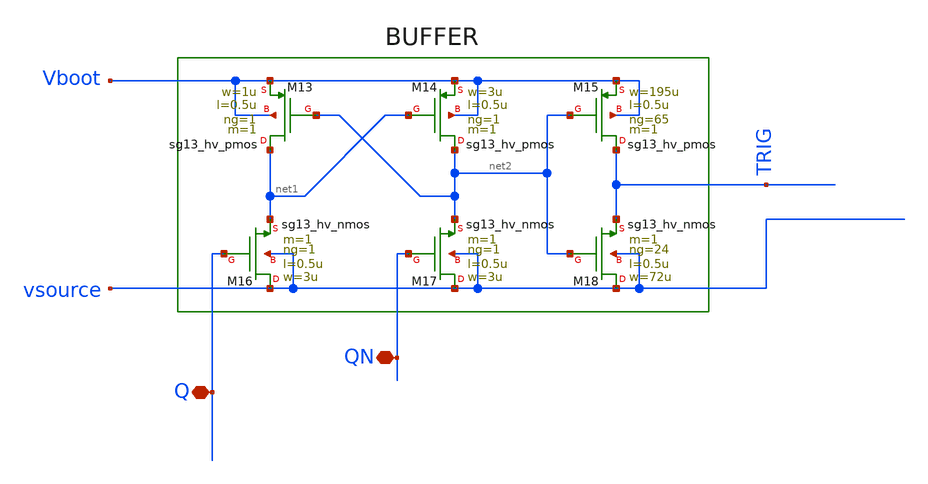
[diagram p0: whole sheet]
** sch_path: xschem/Floating_Gate/BUFFER.sch
**.subckt BUFFER Q QN
*.iopin Q
*.iopin QN
XM13 net1 net2 Vboot Vboot sg13_hv_pmos w=1u l=0.5u ng=1 m=1 mm_ok=1
XM14 net2 net1 Vboot Vboot sg13_hv_pmos w=3u l=0.5u ng=1 m=1 mm_ok=1
XM15 TRIG net2 Vboot Vboot sg13_hv_pmos w=195u l=0.5u ng=65 m=1 mm_ok=1
XM16 vsource Q net1 vsource sg13_hv_nmos w=3u l=0.5u ng=1 m=1 mm_ok=1
XM17 vsource QN net2 vsource sg13_hv_nmos w=3u l=0.5u ng=1 m=1 mm_ok=1
XM18 vsource net2 TRIG vsource sg13_hv_nmos w=72u l=0.5u ng=24 m=1 mm_ok=1
**.ends
.end
